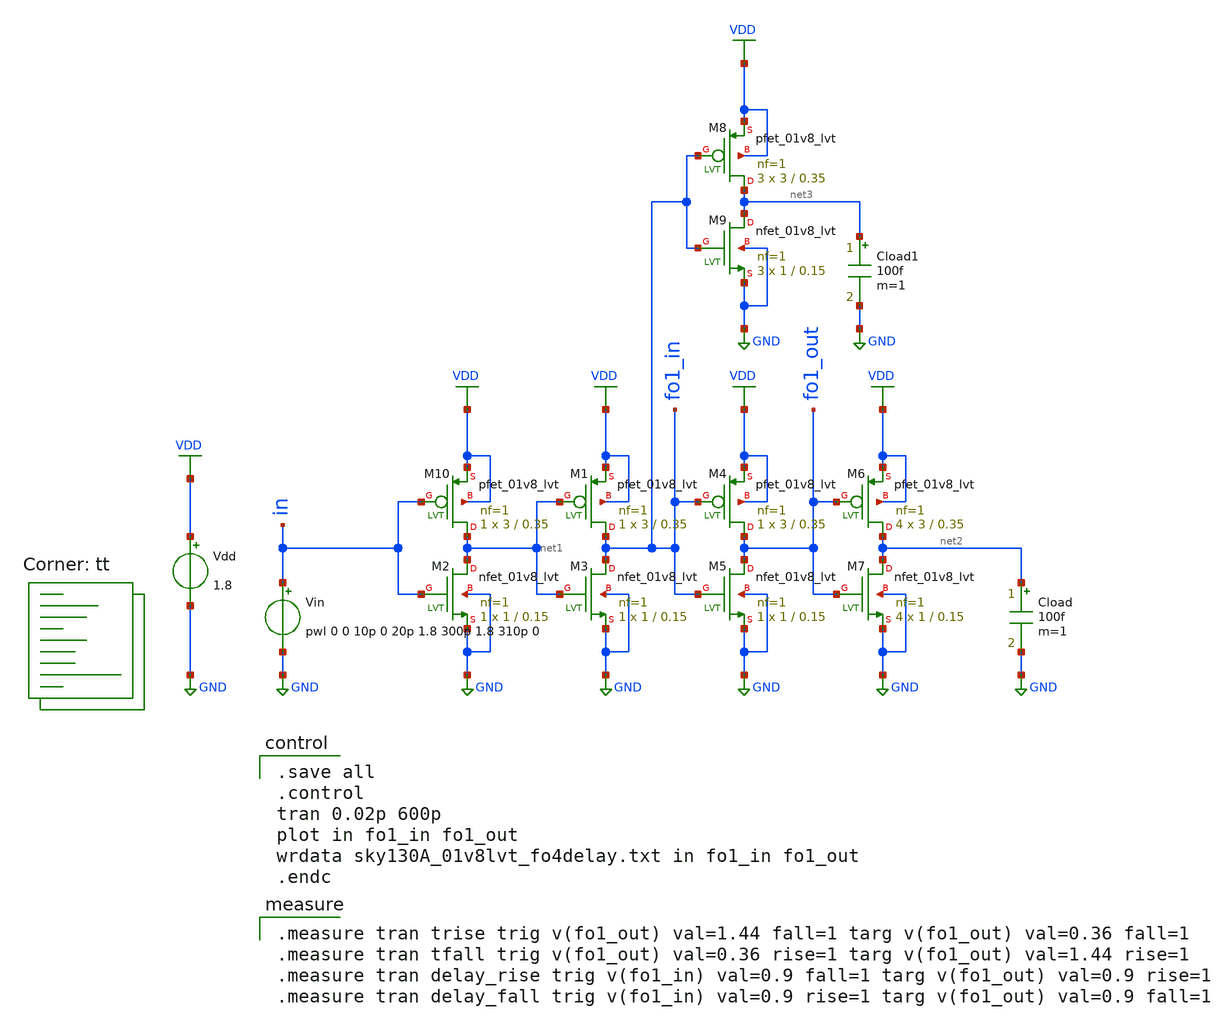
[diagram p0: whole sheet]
** sch_path: xschem/Logic/sky130A_01v8lvt_fo4delay.sch
* Copyright 2021 Stefan Frederik Schippers
* Licensed under the Apache License, Version 2.0 (the "License");
* you may not use this file except in compliance with the License.
* You may obtain a copy of the License at
* https://www.apache.org/licenses/LICENSE-2.0
* Unless required by applicable law or agreed to in writing, software
* distributed under the License is distributed on an "AS IS" BASIS,
* WITHOUT WARRANTIES OR CONDITIONS OF ANY KIND, either express or implied.
* See the License for the specific language governing permissions and
* limitations under the License.
**.subckt sky130A_01v8lvt_fo4delay
Vdd VDD GND 1.8
Vin in GND pwl 0 0 10p 0 20p 1.8 300p 1.8 310p 0
Cload net2 GND 100f m=1
Cload1 net3 GND 100f m=1
XM10 net1 in VDD VDD sky130_fd_pr__pfet_01v8_lvt L=0.35 W=3 nf=1 ad='int((1 + 1)/2) * 3 / 1 * 0.29' as='int((1 + 2)/2) * 3 / 1 * 0.29'
+ pd='2*int((1 + 1)/2) * (3 / 1 + 0.29)' ps='2*int((1 + 2)/2) * (3 / 1 + 0.29)' nrd='0.29 / 3 ' nrs='0.29 / 3 '
+ sa=0 sb=0 sd=0 mult=1 m=1
XM2 net1 in GND GND sky130_fd_pr__nfet_01v8_lvt L=0.15 W=1 nf=1 ad='int((1 + 1)/2) * 1 / 1 * 0.29' as='int((1 + 2)/2) * 1 / 1 * 0.29'
+ pd='2*int((1 + 1)/2) * (1 / 1 + 0.29)' ps='2*int((1 + 2)/2) * (1 / 1 + 0.29)' nrd='0.29 / 1 ' nrs='0.29 / 1 '
+ sa=0 sb=0 sd=0 mult=1 m=1
XM1 fo1_in net1 VDD VDD sky130_fd_pr__pfet_01v8_lvt L=0.35 W=3 nf=1 ad='int((1 + 1)/2) * 3 / 1 * 0.29'
+ as='int((1 + 2)/2) * 3 / 1 * 0.29' pd='2*int((1 + 1)/2) * (3 / 1 + 0.29)' ps='2*int((1 + 2)/2) * (3 / 1 + 0.29)'
+ nrd='0.29 / 3 ' nrs='0.29 / 3 ' sa=0 sb=0 sd=0 mult=1 m=1
XM3 fo1_in net1 GND GND sky130_fd_pr__nfet_01v8_lvt L=0.15 W=1 nf=1 ad='int((1 + 1)/2) * 1 / 1 * 0.29'
+ as='int((1 + 2)/2) * 1 / 1 * 0.29' pd='2*int((1 + 1)/2) * (1 / 1 + 0.29)' ps='2*int((1 + 2)/2) * (1 / 1 + 0.29)'
+ nrd='0.29 / 1 ' nrs='0.29 / 1 ' sa=0 sb=0 sd=0 mult=1 m=1
XM4 fo1_out fo1_in VDD VDD sky130_fd_pr__pfet_01v8_lvt L=0.35 W=3 nf=1 ad='int((1 + 1)/2) * 3 / 1 * 0.29'
+ as='int((1 + 2)/2) * 3 / 1 * 0.29' pd='2*int((1 + 1)/2) * (3 / 1 + 0.29)' ps='2*int((1 + 2)/2) * (3 / 1 + 0.29)'
+ nrd='0.29 / 3 ' nrs='0.29 / 3 ' sa=0 sb=0 sd=0 mult=1 m=1
XM5 fo1_out fo1_in GND GND sky130_fd_pr__nfet_01v8_lvt L=0.15 W=1 nf=1 ad='int((1 + 1)/2) * 1 / 1 * 0.29'
+ as='int((1 + 2)/2) * 1 / 1 * 0.29' pd='2*int((1 + 1)/2) * (1 / 1 + 0.29)' ps='2*int((1 + 2)/2) * (1 / 1 + 0.29)'
+ nrd='0.29 / 1 ' nrs='0.29 / 1 ' sa=0 sb=0 sd=0 mult=1 m=1
XM6 net2 fo1_out VDD VDD sky130_fd_pr__pfet_01v8_lvt L=0.35 W=3 nf=1 ad='int((1 + 1)/2) * 3 / 1 * 0.29'
+ as='int((1 + 2)/2) * 3 / 1 * 0.29' pd='2*int((1 + 1)/2) * (3 / 1 + 0.29)' ps='2*int((1 + 2)/2) * (3 / 1 + 0.29)'
+ nrd='0.29 / 3 ' nrs='0.29 / 3 ' sa=0 sb=0 sd=0 mult=4 m=4
XM7 net2 fo1_out GND GND sky130_fd_pr__nfet_01v8_lvt L=0.15 W=1 nf=1 ad='int((1 + 1)/2) * 1 / 1 * 0.29'
+ as='int((1 + 2)/2) * 1 / 1 * 0.29' pd='2*int((1 + 1)/2) * (1 / 1 + 0.29)' ps='2*int((1 + 2)/2) * (1 / 1 + 0.29)'
+ nrd='0.29 / 1 ' nrs='0.29 / 1 ' sa=0 sb=0 sd=0 mult=4 m=4
XM8 net3 fo1_in VDD VDD sky130_fd_pr__pfet_01v8_lvt L=0.35 W=3 nf=1 ad='int((1 + 1)/2) * 3 / 1 * 0.29'
+ as='int((1 + 2)/2) * 3 / 1 * 0.29' pd='2*int((1 + 1)/2) * (3 / 1 + 0.29)' ps='2*int((1 + 2)/2) * (3 / 1 + 0.29)'
+ nrd='0.29 / 3 ' nrs='0.29 / 3 ' sa=0 sb=0 sd=0 mult=3 m=3
XM9 net3 fo1_in GND GND sky130_fd_pr__nfet_01v8_lvt L=0.15 W=1 nf=1 ad='int((1 + 1)/2) * 1 / 1 * 0.29'
+ as='int((1 + 2)/2) * 1 / 1 * 0.29' pd='2*int((1 + 1)/2) * (1 / 1 + 0.29)' ps='2*int((1 + 2)/2) * (1 / 1 + 0.29)'
+ nrd='0.29 / 1 ' nrs='0.29 / 1 ' sa=0 sb=0 sd=0 mult=3 m=3
**** begin user architecture code
.lib $::SKYWATER_MODELS/sky130.lib.spice tt

.save all
.control
tran 0.02p 600p
plot in fo1_in fo1_out
wrdata sky130A_01v8lvt_fo4delay.txt in fo1_in fo1_out
.endc


.measure tran trise trig v(fo1_out) val=1.44 fall=1 targ v(fo1_out) val=0.36 fall=1
.measure tran tfall trig v(fo1_out) val=0.36 rise=1 targ v(fo1_out) val=1.44 rise=1
.measure tran delay_rise trig v(fo1_in) val=0.9 fall=1 targ v(fo1_out) val=0.9 rise=1
.measure tran delay_fall trig v(fo1_in) val=0.9 rise=1 targ v(fo1_out) val=0.9 fall=1

**** end user architecture code
**.ends
.GLOBAL VDD
.GLOBAL GND
.end
